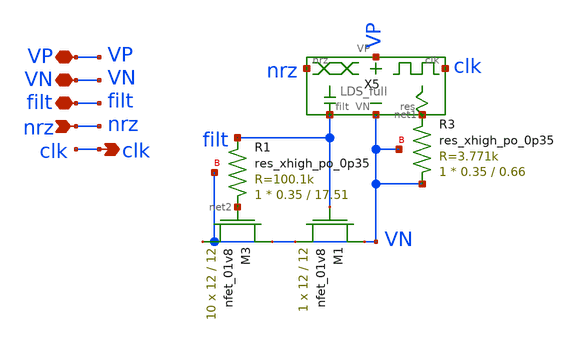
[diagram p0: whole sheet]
** sch_path: LDS/LDS_pasdpll.sch
**.subckt LDS_pasdpll VN VP nrz filt clk
*.iopin VN
*.iopin VP
*.ipin nrz
*.iopin filt
*.opin clk
X5 VP VN filt nrz net1 clk LDS_full
XM3 VN net2 VN VN sky130_fd_pr__nfet_01v8 L=12 W=12 nf=1 ad='int((nf+1)/2) * W/nf * 0.29' as='int((nf+2)/2) * W/nf * 0.29'
+ pd='2*int((nf+1)/2) * (W/nf + 0.29)' ps='2*int((nf+2)/2) * (W/nf + 0.29)' nrd='0.29 / W' nrs='0.29 / W'
+ sa=0 sb=0 sd=0 mult=10 m=10
XM1 VN filt VN VN sky130_fd_pr__nfet_01v8 L=12 W=12 nf=1 ad='int((nf+1)/2) * W/nf * 0.29' as='int((nf+2)/2) * W/nf * 0.29'
+ pd='2*int((nf+1)/2) * (W/nf + 0.29)' ps='2*int((nf+2)/2) * (W/nf + 0.29)' nrd='0.29 / W' nrs='0.29 / W'
+ sa=0 sb=0 sd=0 mult=1 m=1
XR3 VN net1 VN sky130_fd_pr__res_xhigh_po_0p35 W=0.35 L=0.66 mult=1 m=1
XR1 net2 filt VN sky130_fd_pr__res_xhigh_po_0p35 W=0.35 L=17.51 mult=1 m=1
**.ends
.end
